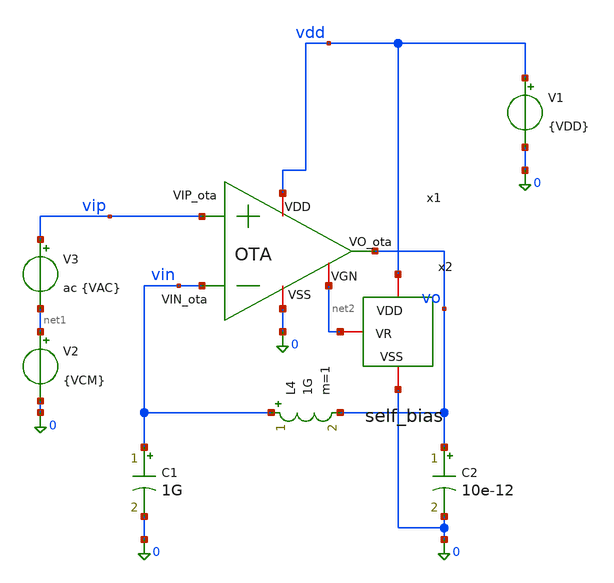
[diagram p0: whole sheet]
** sch_path: xschem/OTA/OTA_tb.sch
**.subckt OTA_tb
x1 vdd vo vin vip 0 net2 OTA
V1 vdd 0 {VDD}
V2 net1 0 {VCM}
V3 vip net1 ac {VAC}
C1 vin 0 1G m=1
L4 vin vo 1G m=1
C2 vo 0 10e-12 m=1
x2 vdd net2 0 self_bias
**** begin user architecture code




* 1. Inclusión de libreria de modelos Sky130 PRIMERO
.lib /foss/pdks/sky130A/libs.tech/ngspice/sky130.lib.spice ss
.include /foss/designs/LDO-sky130/xschem/OTA/OTA_pex.spice
.option temp=120

**parametros_ota
.param VDD = 1.8
.param VCM = 0.6
.param VAC = 1



.control

save all
* PMOS
* --- Circuito de Polarización (Referencia) ---


* --- Etapa Diferencial (Núcleo del OTA) ---

* Mrc1 (pfet_01v8_lvt)
save @m.x1.xMrc1.msky130_fd_pr__pfet_01v8_lvt[gm]
save @m.x1.xMrc1.msky130_fd_pr__pfet_01v8_lvt[gds]
save @m.x1.xMrc1.msky130_fd_pr__pfet_01v8_lvt[id]
save @m.x1.xMrc1.msky130_fd_pr__pfet_01v8_lvt[vgs]
save @m.x1.xMrc1.msky130_fd_pr__pfet_01v8_lvt[vds]
save @m.x1.xMrc1.msky130_fd_pr__pfet_01v8_lvt[vth]
save @m.x1.xMrc1.msky130_fd_pr__pfet_01v8_lvt[vdsat]

* Mn (pfet_01v8)
save @m.x1.xMn.msky130_fd_pr__pfet_01v8_lvt[gm]
save @m.x1.xMn.msky130_fd_pr__pfet_01v8_lvt[gds]
save @m.x1.xMn.msky130_fd_pr__pfet_01v8_lvt[id]
save @m.x1.xMn.msky130_fd_pr__pfet_01v8_lvt[vgs]
save @m.x1.xMn.msky130_fd_pr__pfet_01v8_lvt[vds]
save @m.x1.xMn.msky130_fd_pr__pfet_01v8_lvt[vth]
save @m.x1.xMn.msky130_fd_pr__pfet_01v8_lvt[vdsat]

* Mp (pfet_01v8)
save @m.x1.xMp.msky130_fd_pr__pfet_01v8_lvt[gm]
save @m.x1.xMp.msky130_fd_pr__pfet_01v8_lvt[gds]
save @m.x1.xMp.msky130_fd_pr__pfet_01v8_lvt[id]
save @m.x1.xMp.msky130_fd_pr__pfet_01v8_lvt[vgs]
save @m.x1.xMp.msky130_fd_pr__pfet_01v8_lvt[vds]
save @m.x1.xMp.msky130_fd_pr__pfet_01v8_lvt[vth]
save @m.x1.xMp.msky130_fd_pr__pfet_01v8_lvt[vdsat]

* Mnr (nfet_01v8)
save @m.x1.xMnr.msky130_fd_pr__nfet_01v8[gm]
save @m.x1.xMnr.msky130_fd_pr__nfet_01v8[gds]
save @m.x1.xMnr.msky130_fd_pr__nfet_01v8[id]
save @m.x1.xMnr.msky130_fd_pr__nfet_01v8[vgs]
save @m.x1.xMnr.msky130_fd_pr__nfet_01v8[vds]
save @m.x1.xMnr.msky130_fd_pr__nfet_01v8[vth]
save @m.x1.xMnr.msky130_fd_pr__nfet_01v8[vdsat]

* Mpr (nfet_01v8)
save @m.x1.xMpr.msky130_fd_pr__nfet_01v8[gm]
save @m.x1.xMpr.msky130_fd_pr__nfet_01v8[gds]
save @m.x1.xMpr.msky130_fd_pr__nfet_01v8[id]
save @m.x1.xMpr.msky130_fd_pr__nfet_01v8[vgs]
save @m.x1.xMpr.msky130_fd_pr__nfet_01v8[vds]
save @m.x1.xMpr.msky130_fd_pr__nfet_01v8[vth]
save @m.x1.xMpr.msky130_fd_pr__nfet_01v8[vdsat]


* --- Etapa de Salida ---

* Mrc2 (pfet_01v8_lvt)
save @m.x1.xMrc2.msky130_fd_pr__pfet_01v8_lvt[gm]
save @m.x1.xMrc2.msky130_fd_pr__pfet_01v8_lvt[gds]
save @m.x1.xMrc2.msky130_fd_pr__pfet_01v8_lvt[id]
save @m.x1.xMrc2.msky130_fd_pr__pfet_01v8_lvt[vgs]
save @m.x1.xMrc2.msky130_fd_pr__pfet_01v8_lvt[vds]
save @m.x1.xMrc2.msky130_fd_pr__pfet_01v8_lvt[vth]
save @m.x1.xMrc2.msky130_fd_pr__pfet_01v8_lvt[vdsat]

* Mo (nfet_01v8)
save @m.x1.xMo.msky130_fd_pr__nfet_01v8[gm]
save @m.x1.xMo.msky130_fd_pr__nfet_01v8[gds]
save @m.x1.xMo.msky130_fd_pr__nfet_01v8[id]
save @m.x1.xMo.msky130_fd_pr__nfet_01v8[vgs]
save @m.x1.xMo.msky130_fd_pr__nfet_01v8[vds]
save @m.x1.xMo.msky130_fd_pr__nfet_01v8[vth]
save @m.x1.xMo.msky130_fd_pr__nfet_01v8[vdsat]

set filetype=ascii
op
write OTA_op.raw


ac dec 10 1 1G
write OTA_ac.raw


* 1. Frecuencia de Corte a -3dB
meas ac f3db WHEN vdb(vo) = vdb(vo)[0] - 3

* 2. UGB (Frecuencia donde la magnitud cruza 0 dB)
meas ac ugb WHEN vdb(vo) = 0

* 3. Crear el vector de fase y convertirlo a grados (multiplicando por 180/pi)
let fase_deg = cph(v(vo)) * 180 / pi

* 4. Medir la fase en grados en el punto exacto del UGB
meas ac fase_ugb FIND fase_deg WHEN vdb(vo) = 0

* 5. Calcular el Margen de Fase automáticamente
let margen_fase = 180 + fase_ugb

meas ac ganancia_banda_plana   find vdb(vo) at=10

print margen_fase
print ac ganancia_banda_plana

* 6. Graficar la magnitud y la fase ya convertida a grados
plot vdb(vo)
plot fase_deg
.endc


**** end user architecture code
**.ends

* expanding   symbol:  /foss/designs/LDO-sky130/xschem/OTA/OTA.sym # of pins=6
** sym_path: xschem/OTA/OTA.sym
** sch_path: xschem/OTA/OTA.sch
.subckt OTA VDD VO_ota VIN_ota VIP_ota VSS VGN
*.ipin VIN_ota
*.opin VO_ota
*.iopin VSS
*.iopin VDD
*.ipin VIP_ota
*.iopin VGN
XMpr vo1 vd VSS VSS sky130_fd_pr__nfet_01v8 L=1 W=6 nf=4 ad='int((4 + 1)/2) * 6 / 4 * 0.29' as='int((4 + 2)/2) * 6 / 4 * 0.29'
+ pd='2*int((4 + 1)/2) * (6 / 4 + 0.29)' ps='2*int((4 + 2)/2) * (6 / 4 + 0.29)' nrd='0.29 / 6 ' nrs='0.29 / 6 '
+ sa=0 sb=0 sd=0 mult=1 m=1
XMnr vd vd VSS VSS sky130_fd_pr__nfet_01v8 L=1 W=6 nf=4 ad='int((4 + 1)/2) * 6 / 4 * 0.29' as='int((4 + 2)/2) * 6 / 4 * 0.29'
+ pd='2*int((4 + 1)/2) * (6 / 4 + 0.29)' ps='2*int((4 + 2)/2) * (6 / 4 + 0.29)' nrd='0.29 / 6 ' nrs='0.29 / 6 '
+ sa=0 sb=0 sd=0 mult=1 m=1
XMo VO_ota vo1 VSS VSS sky130_fd_pr__nfet_01v8 L=2 W=8 nf=8 ad='int((8 + 1)/2) * 8 / 8 * 0.29' as='int((8 + 2)/2) * 8 / 8 * 0.29'
+ pd='2*int((8 + 1)/2) * (8 / 8 + 0.29)' ps='2*int((8 + 2)/2) * (8 / 8 + 0.29)' nrd='0.29 / 8 ' nrs='0.29 / 8 '
+ sa=0 sb=0 sd=0 mult=1 m=1
XMrc2 VO_ota vgp VDD VDD sky130_fd_pr__pfet_01v8_lvt L=2 W=50 nf=8 ad='int((8 + 1)/2) * 50 / 8 * 0.29'
+ as='int((8 + 2)/2) * 50 / 8 * 0.29' pd='2*int((8 + 1)/2) * (50 / 8 + 0.29)' ps='2*int((8 + 2)/2) * (50 / 8 + 0.29)'
+ nrd='0.29 / 50 ' nrs='0.29 / 50 ' sa=0 sb=0 sd=0 mult=1 m=1
XC1 VO_ota vmiler sky130_fd_pr__cap_mim_m3_2 W=44.6 L=56 MF=1 m=1
XMp vo1 VIP_ota vtail VDD sky130_fd_pr__pfet_01v8_lvt L=1 W=26 nf=4 ad='int((4 + 1)/2) * 26 / 4 * 0.29'
+ as='int((4 + 2)/2) * 26 / 4 * 0.29' pd='2*int((4 + 1)/2) * (26 / 4 + 0.29)' ps='2*int((4 + 2)/2) * (26 / 4 + 0.29)'
+ nrd='0.29 / 26 ' nrs='0.29 / 26 ' sa=0 sb=0 sd=0 mult=1 m=1
XMn vd VIN_ota vtail VDD sky130_fd_pr__pfet_01v8_lvt L=1 W=26 nf=4 ad='int((4 + 1)/2) * 26 / 4 * 0.29'
+ as='int((4 + 2)/2) * 26 / 4 * 0.29' pd='2*int((4 + 1)/2) * (26 / 4 + 0.29)' ps='2*int((4 + 2)/2) * (26 / 4 + 0.29)'
+ nrd='0.29 / 26 ' nrs='0.29 / 26 ' sa=0 sb=0 sd=0 mult=1 m=1
XMrc1 vtail vgp VDD VDD sky130_fd_pr__pfet_01v8_lvt L=1 W=50 nf=8 ad='int((8 + 1)/2) * 50 / 8 * 0.29'
+ as='int((8 + 2)/2) * 50 / 8 * 0.29' pd='2*int((8 + 1)/2) * (50 / 8 + 0.29)' ps='2*int((8 + 2)/2) * (50 / 8 + 0.29)'
+ nrd='0.29 / 50 ' nrs='0.29 / 50 ' sa=0 sb=0 sd=0 mult=1 m=1
XMr vgp vgp VDD VDD sky130_fd_pr__pfet_01v8_lvt L=1 W=12.5 nf=2 ad='int((2 + 1)/2) * 12.5 / 2 * 0.29'
+ as='int((2 + 2)/2) * 12.5 / 2 * 0.29' pd='2*int((2 + 1)/2) * (12.5 / 2 + 0.29)' ps='2*int((2 + 2)/2) * (12.5 / 2 + 0.29)'
+ nrd='0.29 / 12.5 ' nrs='0.29 / 12.5 ' sa=0 sb=0 sd=0 mult=1 m=1
XMnref vgp VGN VSS VSS sky130_fd_pr__nfet_01v8 L=1 W=8 nf=1 ad='int((1 + 1)/2) * 8 / 1 * 0.29' as='int((1 + 2)/2) * 8 / 1 * 0.29'
+ pd='2*int((1 + 1)/2) * (8 / 1 + 0.29)' ps='2*int((1 + 2)/2) * (8 / 1 + 0.29)' nrd='0.29 / 8 ' nrs='0.29 / 8 '
+ sa=0 sb=0 sd=0 mult=1 m=1
XR10 vo1 vmiler VSS sky130_fd_pr__res_xhigh_po_0p35 L=90.72 mult=1 m=1
.ends


* expanding   symbol:  /foss/designs/LDO-sky130/xschem/Self_Bias/self_bias.sym # of pins=3
** sym_path: xschem/Iref/self_bias.sym
** sch_path: xschem/Iref/self_bias.sch
.subckt self_bias VDD VR VSS
*.iopin VR
*.iopin VDD
*.iopin VSS
XMp4 vgp_self vgp_self VDD VDD sky130_fd_pr__pfet_01v8_lvt L=1 W=30 nf=6 ad='int((6 + 1)/2) * 30 / 6 * 0.29'
+ as='int((6 + 2)/2) * 30 / 6 * 0.29' pd='2*int((6 + 1)/2) * (30 / 6 + 0.29)' ps='2*int((6 + 2)/2) * (30 / 6 + 0.29)'
+ nrd='0.29 / 30 ' nrs='0.29 / 30 ' sa=0 sb=0 sd=0 mult=1 m=1
XMp3 VDI vgp_self VDD VDD sky130_fd_pr__pfet_01v8_lvt L=1 W=30 nf=6 ad='int((6 + 1)/2) * 30 / 6 * 0.29'
+ as='int((6 + 2)/2) * 30 / 6 * 0.29' pd='2*int((6 + 1)/2) * (30 / 6 + 0.29)' ps='2*int((6 + 2)/2) * (30 / 6 + 0.29)'
+ nrd='0.29 / 30 ' nrs='0.29 / 30 ' sa=0 sb=0 sd=0 mult=1 m=1
XMs2 VDinv VR vp1 VDD sky130_fd_pr__pfet_01v8_lvt L=5 W=0.5 nf=1 ad='int((1 + 1)/2) * 0.5 / 1 * 0.29'
+ as='int((1 + 2)/2) * 0.5 / 1 * 0.29' pd='2*int((1 + 1)/2) * (0.5 / 1 + 0.29)' ps='2*int((1 + 2)/2) * (0.5 / 1 + 0.29)'
+ nrd='0.29 / 0.5 ' nrs='0.29 / 0.5 ' sa=0 sb=0 sd=0 mult=1 m=1
XMn2 vgp_self VDI VR VSS sky130_fd_pr__nfet_01v8 L=1 W=24 nf=6 ad='int((6 + 1)/2) * 24 / 6 * 0.29' as='int((6 + 2)/2) * 24 / 6 * 0.29'
+ pd='2*int((6 + 1)/2) * (24 / 6 + 0.29)' ps='2*int((6 + 2)/2) * (24 / 6 + 0.29)' nrd='0.29 / 24 ' nrs='0.29 / 24 '
+ sa=0 sb=0 sd=0 mult=1 m=1
XMn1 VDI VR VSS VSS sky130_fd_pr__nfet_01v8 L=1 W=5 nf=5 ad='int((5 + 1)/2) * 5 / 5 * 0.29' as='int((5 + 2)/2) * 5 / 5 * 0.29'
+ pd='2*int((5 + 1)/2) * (5 / 5 + 0.29)' ps='2*int((5 + 2)/2) * (5 / 5 + 0.29)' nrd='0.29 / 5 ' nrs='0.29 / 5 '
+ sa=0 sb=0 sd=0 mult=1 m=1
XMs3 VDinv VR VSS VSS sky130_fd_pr__nfet_01v8 L=1 W=20 nf=5 ad='int((5 + 1)/2) * 20 / 5 * 0.29' as='int((5 + 2)/2) * 20 / 5 * 0.29'
+ pd='2*int((5 + 1)/2) * (20 / 5 + 0.29)' ps='2*int((5 + 2)/2) * (20 / 5 + 0.29)' nrd='0.29 / 20 ' nrs='0.29 / 20 '
+ sa=0 sb=0 sd=0 mult=1 m=1
XMs1 vgp_self VDinv VSS VSS sky130_fd_pr__nfet_01v8 L=1 W=2 nf=2 ad='int((2 + 1)/2) * 2 / 2 * 0.29' as='int((2 + 2)/2) * 2 / 2 * 0.29'
+ pd='2*int((2 + 1)/2) * (2 / 2 + 0.29)' ps='2*int((2 + 2)/2) * (2 / 2 + 0.29)' nrd='0.29 / 2 ' nrs='0.29 / 2 '
+ sa=0 sb=0 sd=0 mult=1 m=1
XR11 VSS VR VSS sky130_fd_pr__res_xhigh_po_0p69 L=20.7 mult=1 m=1
XMs4 vp1 VR vp2 VDD sky130_fd_pr__pfet_01v8_lvt L=5 W=0.5 nf=1 ad='int((1 + 1)/2) * 0.5 / 1 * 0.29' as='int((1 + 2)/2) * 0.5 / 1 * 0.29'
+ pd='2*int((1 + 1)/2) * (0.5 / 1 + 0.29)' ps='2*int((1 + 2)/2) * (0.5 / 1 + 0.29)' nrd='0.29 / 0.5 ' nrs='0.29 / 0.5 '
+ sa=0 sb=0 sd=0 mult=1 m=1
XMs5 vp2 VR vp3 VDD sky130_fd_pr__pfet_01v8_lvt L=5 W=0.5 nf=1 ad='int((1 + 1)/2) * 0.5 / 1 * 0.29' as='int((1 + 2)/2) * 0.5 / 1 * 0.29'
+ pd='2*int((1 + 1)/2) * (0.5 / 1 + 0.29)' ps='2*int((1 + 2)/2) * (0.5 / 1 + 0.29)' nrd='0.29 / 0.5 ' nrs='0.29 / 0.5 '
+ sa=0 sb=0 sd=0 mult=1 m=1
XMs6 vp3 VR vp4 VDD sky130_fd_pr__pfet_01v8_lvt L=5 W=0.5 nf=1 ad='int((1 + 1)/2) * 0.5 / 1 * 0.29' as='int((1 + 2)/2) * 0.5 / 1 * 0.29'
+ pd='2*int((1 + 1)/2) * (0.5 / 1 + 0.29)' ps='2*int((1 + 2)/2) * (0.5 / 1 + 0.29)' nrd='0.29 / 0.5 ' nrs='0.29 / 0.5 '
+ sa=0 sb=0 sd=0 mult=1 m=1
XMs7 vp4 VR VDD VDD sky130_fd_pr__pfet_01v8_lvt L=5 W=0.5 nf=1 ad='int((1 + 1)/2) * 0.5 / 1 * 0.29' as='int((1 + 2)/2) * 0.5 / 1 * 0.29'
+ pd='2*int((1 + 1)/2) * (0.5 / 1 + 0.29)' ps='2*int((1 + 2)/2) * (0.5 / 1 + 0.29)' nrd='0.29 / 0.5 ' nrs='0.29 / 0.5 '
+ sa=0 sb=0 sd=0 mult=1 m=1
.ends

.end
